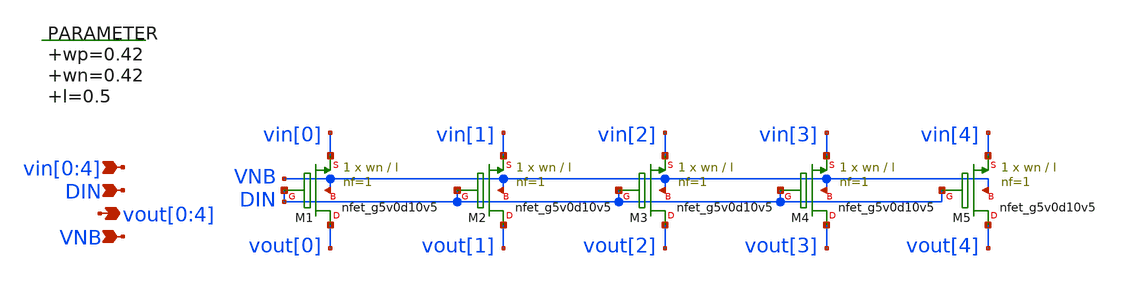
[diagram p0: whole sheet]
** sch_path: xschem/vselector_4b.sch
**.subckt vselector_4b vin[0],vin[1],vin[2],vin[3],vin[4] vout[0],vout[1],vout[2],vout[3],vout[4]
*+ VNB DIN
*.ipin vin[0],vin[1],vin[2],vin[3],vin[4]
*.opin vout[0],vout[1],vout[2],vout[3],vout[4]
*.ipin VNB
*.ipin DIN
.param wp=0.42 wn=0.42 l=0.5

XM1 vout[0] DIN vin[0] VNB sky130_fd_pr__nfet_g5v0d10v5 L=l W=wn nf=1 ad='int((nf+1)/2) * W/nf * 0.29'
+ as='int((nf+2)/2) * W/nf * 0.29' pd='2*int((nf+1)/2) * (W/nf + 0.29)' ps='2*int((nf+2)/2) * (W/nf + 0.29)'
+ nrd='0.29 / W' nrs='0.29 / W' sa=0 sb=0 sd=0 mult=1 m=1
XM2 vout[1] DIN vin[1] VNB sky130_fd_pr__nfet_g5v0d10v5 L=l W=wn nf=1 ad='int((nf+1)/2) * W/nf * 0.29'
+ as='int((nf+2)/2) * W/nf * 0.29' pd='2*int((nf+1)/2) * (W/nf + 0.29)' ps='2*int((nf+2)/2) * (W/nf + 0.29)'
+ nrd='0.29 / W' nrs='0.29 / W' sa=0 sb=0 sd=0 mult=1 m=1
XM3 vout[2] DIN vin[2] VNB sky130_fd_pr__nfet_g5v0d10v5 L=l W=wn nf=1 ad='int((nf+1)/2) * W/nf * 0.29'
+ as='int((nf+2)/2) * W/nf * 0.29' pd='2*int((nf+1)/2) * (W/nf + 0.29)' ps='2*int((nf+2)/2) * (W/nf + 0.29)'
+ nrd='0.29 / W' nrs='0.29 / W' sa=0 sb=0 sd=0 mult=1 m=1
XM4 vout[3] DIN vin[3] VNB sky130_fd_pr__nfet_g5v0d10v5 L=l W=wn nf=1 ad='int((nf+1)/2) * W/nf * 0.29'
+ as='int((nf+2)/2) * W/nf * 0.29' pd='2*int((nf+1)/2) * (W/nf + 0.29)' ps='2*int((nf+2)/2) * (W/nf + 0.29)'
+ nrd='0.29 / W' nrs='0.29 / W' sa=0 sb=0 sd=0 mult=1 m=1
XM5 vout[4] DIN vin[4] VNB sky130_fd_pr__nfet_g5v0d10v5 L=l W=wn nf=1 ad='int((nf+1)/2) * W/nf * 0.29'
+ as='int((nf+2)/2) * W/nf * 0.29' pd='2*int((nf+1)/2) * (W/nf + 0.29)' ps='2*int((nf+2)/2) * (W/nf + 0.29)'
+ nrd='0.29 / W' nrs='0.29 / W' sa=0 sb=0 sd=0 mult=1 m=1
**.ends
.end
